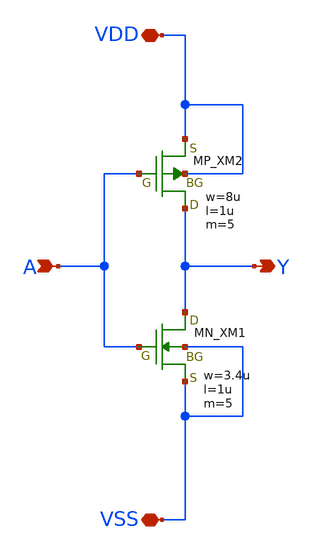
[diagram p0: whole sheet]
** sch_path: schematic/20250924_OSS_Workshop/Qdai/inverter_solo/inv_kawashima.sch
**.subckt inv_kawashima Y A VDD VSS
*.opin Y
*.ipin A
*.iopin VDD
*.iopin VSS
XM2 Y A VDD VDD PMOS w=8u l=1u as=0 ad=0 ps=0 pd=0 nrd=0 nrs=0 m=5
XM1 Y A VSS VSS NMOS w=3.4u l=1u as=0 ad=0 ps=0 pd=0 nrd=0 nrs=0 m=5
**.ends
.end
